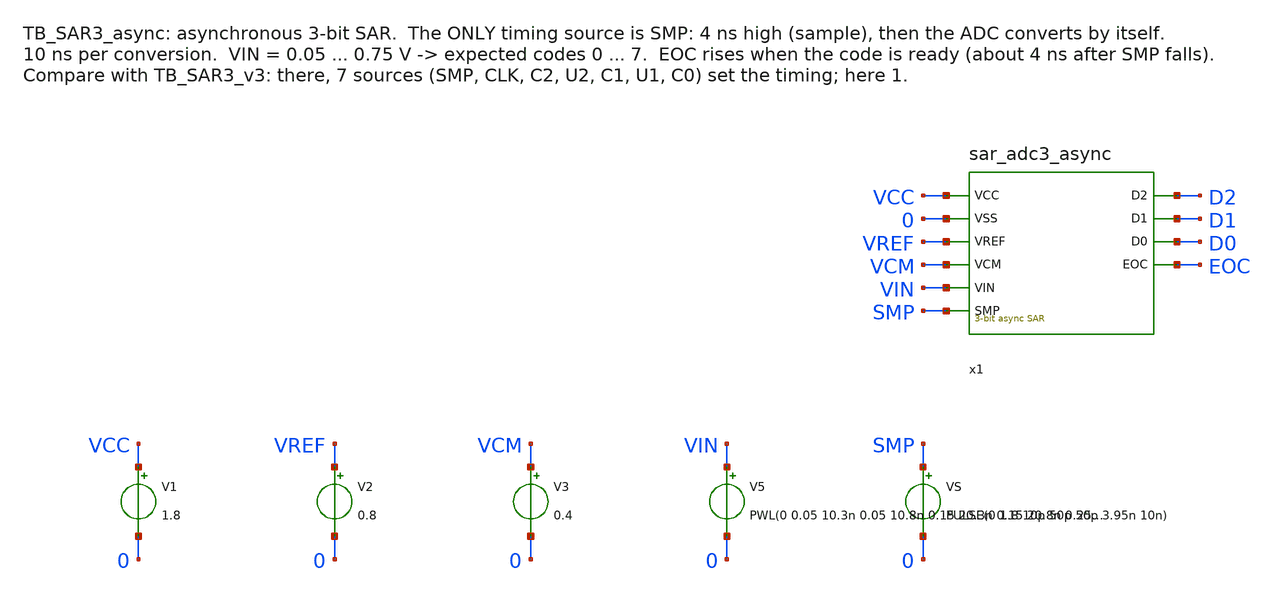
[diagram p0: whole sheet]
** sch_path: SAR_improved/TB_SAR3_async.sch
**.subckt TB_SAR3_async
x1 VCC 0 VREF VCM VIN SMP D2 D1 D0 EOC sar_adc3_async
V1 VCC 0 1.8
V2 VREF 0 0.8
V3 VCM 0 0.4
V5 VIN 0 PWL(0 0.05 10.3n 0.05 10.8n 0.15 20.3n 0.15 20.8n 0.25 30.3n 0.25 30.8n 0.35 40.3n 0.35
+ 40.8n 0.45 50.3n 0.45 50.8n 0.55 60.3n 0.55 60.8n 0.65 70.3n 0.65 70.8n 0.75)
VS SMP 0 PULSE(0 1.8 10p 50p 50p 3.95n 10n)
**** begin user architecture code

.lib /home/ttuser/pdk/sky130A/libs.tech/combined/sky130.lib.spice tt
.option method=gear reltol=1e-4
.control
save all
tran 5p 80n
let code = 4*ceil((v(D2)-0.9)/10) + 2*ceil((v(D1)-0.9)/10) + ceil((v(D0)-0.9)/10)
meas tran code1 find code at=9.9n
meas tran code2 find code at=19.9n
meas tran code3 find code at=29.9n
meas tran code4 find code at=39.9n
meas tran code5 find code at=49.9n
meas tran code6 find code at=59.9n
meas tran code7 find code at=69.9n
meas tran code8 find code at=79.9n
meas tran teoc1 when v(EOC)=0.9 rise=1 from=4n to=10n
meas tran teoc2 when v(EOC)=0.9 rise=1 from=14n to=20n
meas tran teoc3 when v(EOC)=0.9 rise=1 from=24n to=30n
meas tran teoc4 when v(EOC)=0.9 rise=1 from=34n to=40n
meas tran teoc5 when v(EOC)=0.9 rise=1 from=44n to=50n
meas tran teoc6 when v(EOC)=0.9 rise=1 from=54n to=60n
meas tran teoc7 when v(EOC)=0.9 rise=1 from=64n to=70n
meas tran teoc8 when v(EOC)=0.9 rise=1 from=74n to=80n
let ptot = 1.8*(-i(V1)) + 0.8*(-i(V2)) + 0.4*(-i(V3))
meas tran etot integ ptot from=0 to=80n
let e_conv_pJ = etot/8*1e12
let p_uW = etot/80e-9*1e6
print e_conv_pJ p_uW
* conversion time of each code = teocN - (start of period N + SMP width)
plot v(VIN) v(x1.VX) v(x1.VR)
plot v(SMP) v(x1.CLK)+2 v(x1.XB)+4 v(x1.YB)+6 v(EOC)+8
plot v(D2) v(D1)+2 v(D0)+4 v(EOC)+6
plot v(x1.x2.BPA) v(x1.x2.BPB)
plot code v(VIN)
.endc

**** end user architecture code
**.ends
.end
